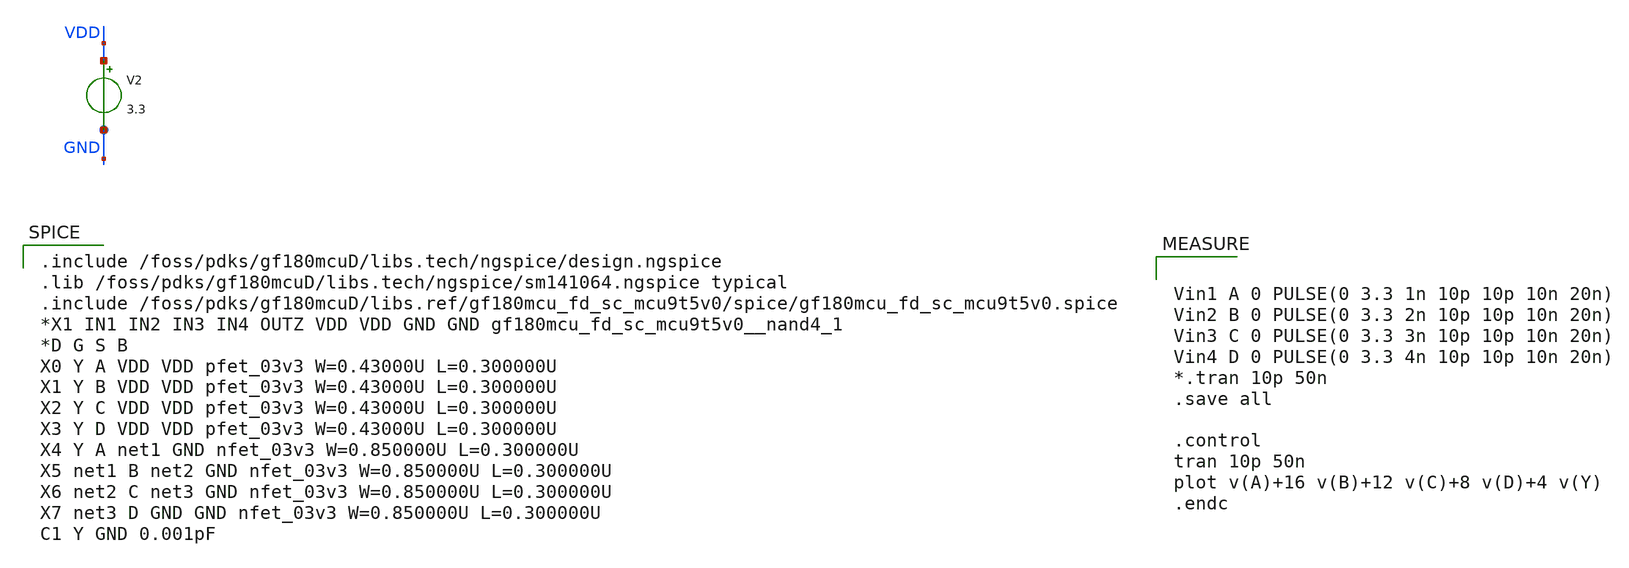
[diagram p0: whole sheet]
** sch_path: designs/libs/tb_NAND4/nand4_test_functional.sch
**.subckt nand4_test_functional
V2 VDD GND 3.3
**** begin user architecture code

.include /foss/pdks/gf180mcuD/libs.tech/ngspice/design.ngspice
.lib /foss/pdks/gf180mcuD/libs.tech/ngspice/sm141064.ngspice typical
.include /foss/pdks/gf180mcuD/libs.ref/gf180mcu_fd_sc_mcu9t5v0/spice/gf180mcu_fd_sc_mcu9t5v0.spice
*X1 IN1 IN2 IN3 IN4 OUTZ VDD VDD GND GND gf180mcu_fd_sc_mcu9t5v0__nand4_1
*D G S B
X0 Y A VDD VDD pfet_03v3 W=0.43000U L=0.300000U
X1 Y B VDD VDD pfet_03v3 W=0.43000U L=0.300000U
X2 Y C VDD VDD pfet_03v3 W=0.43000U L=0.300000U
X3 Y D VDD VDD pfet_03v3 W=0.43000U L=0.300000U
X4 Y A net1 GND nfet_03v3 W=0.850000U L=0.300000U
X5 net1 B net2 GND nfet_03v3 W=0.850000U L=0.300000U
X6 net2 C net3 GND nfet_03v3 W=0.850000U L=0.300000U
X7 net3 D GND GND nfet_03v3 W=0.850000U L=0.300000U
C1 Y GND 0.001pF






Vin1 A 0 PULSE(0 3.3 1n 10p 10p 10n 20n)
Vin2 B 0 PULSE(0 3.3 2n 10p 10p 10n 20n)
Vin3 C 0 PULSE(0 3.3 3n 10p 10p 10n 20n)
Vin4 D 0 PULSE(0 3.3 4n 10p 10p 10n 20n)
*.tran 10p 50n
.save all

.control
tran 10p 50n
plot v(A)+16 v(B)+12 v(C)+8 v(D)+4 v(Y)
.endc



**** end user architecture code
**.ends
.end
